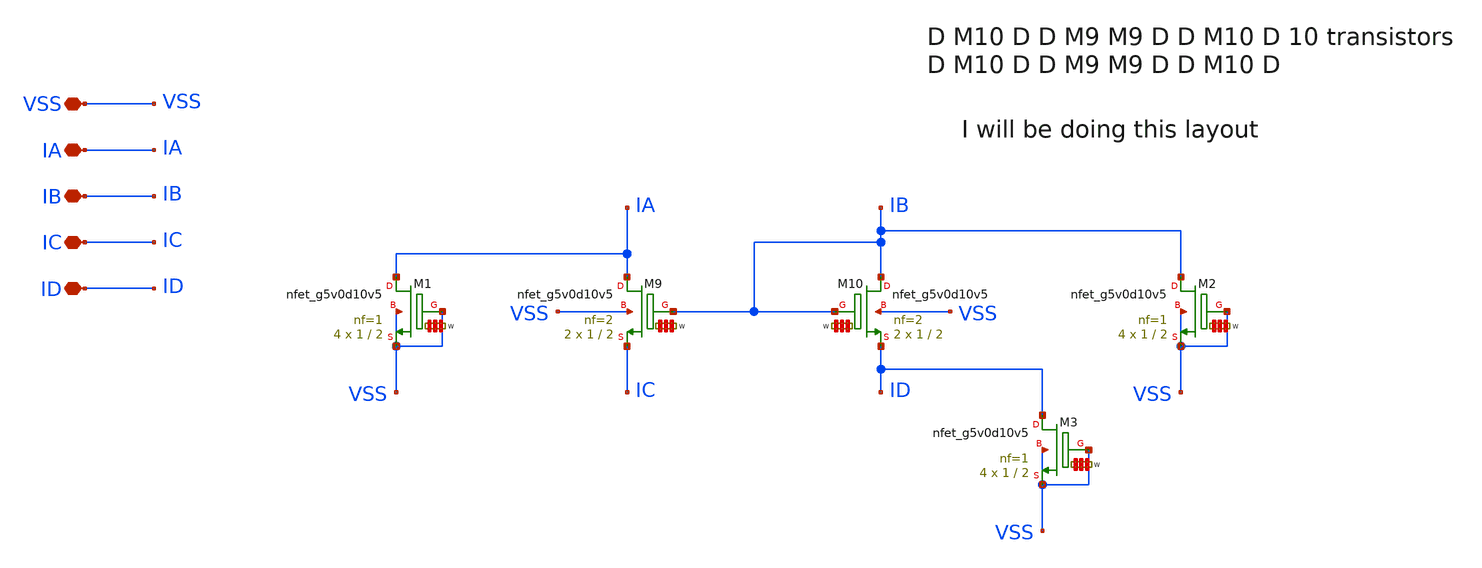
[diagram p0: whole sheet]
** sch_path: Learning/single_ended_amplifiers/Design_and_Analysis_of_Two-Stage_CMOS_Operational_Amplifier_for_Fluorescence_Signal_Processing_sky130_5V/layout/upper_nmos_current_mirror.sch
**.subckt upper_nmos_current_mirror VSS IA IB IC ID
*.iopin VSS
*.iopin IA
*.iopin IB
*.iopin IC
*.iopin ID
XM9 IA IB IC VSS sky130_fd_pr__nfet_g5v0d10v5 L=2 W='1 * 2 ' nf=2 ad='int((nf+1)/2) * W / nf * 0.29'
+ as='int((nf+2)/2) * W / nf * 0.29' pd='2*int((nf+1)/2) * (W / nf + 0.29)' ps='2*int((nf+2)/2) * (W / nf + 0.29)'
+ nrd='0.29 / W ' nrs='0.29 / W ' sa=0 sb=0 sd=0 mult=2 m=2
XM10 IB IB ID VSS sky130_fd_pr__nfet_g5v0d10v5 L=2 W='1 * 2 ' nf=2 ad='int((nf+1)/2) * W / nf * 0.29'
+ as='int((nf+2)/2) * W / nf * 0.29' pd='2*int((nf+1)/2) * (W / nf + 0.29)' ps='2*int((nf+2)/2) * (W / nf + 0.29)'
+ nrd='0.29 / W ' nrs='0.29 / W ' sa=0 sb=0 sd=0 mult=2 m=2
XM1 IA VSS VSS VSS sky130_fd_pr__nfet_g5v0d10v5 L=2 W='1 * 1 ' nf=1 ad='int((nf+1)/2) * W / nf * 0.29'
+ as='int((nf+2)/2) * W / nf * 0.29' pd='2*int((nf+1)/2) * (W / nf + 0.29)' ps='2*int((nf+2)/2) * (W / nf + 0.29)'
+ nrd='0.29 / W ' nrs='0.29 / W ' sa=0 sb=0 sd=0 mult=4 m=4
XM2 IB VSS VSS VSS sky130_fd_pr__nfet_g5v0d10v5 L=2 W='1 * 1 ' nf=1 ad='int((nf+1)/2) * W / nf * 0.29'
+ as='int((nf+2)/2) * W / nf * 0.29' pd='2*int((nf+1)/2) * (W / nf + 0.29)' ps='2*int((nf+2)/2) * (W / nf + 0.29)'
+ nrd='0.29 / W ' nrs='0.29 / W ' sa=0 sb=0 sd=0 mult=4 m=4
XM3 ID VSS VSS VSS sky130_fd_pr__nfet_g5v0d10v5 L=2 W='1 * 1 ' nf=1 ad='int((nf+1)/2) * W / nf * 0.29'
+ as='int((nf+2)/2) * W / nf * 0.29' pd='2*int((nf+1)/2) * (W / nf + 0.29)' ps='2*int((nf+2)/2) * (W / nf + 0.29)'
+ nrd='0.29 / W ' nrs='0.29 / W ' sa=0 sb=0 sd=0 mult=4 m=4
**.ends
.end
